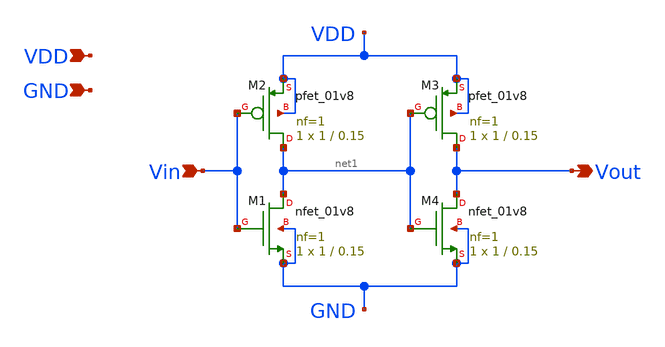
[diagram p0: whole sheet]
** sch_path: xschem/untitled-1.sch
**.subckt untitled-1 Vin VDD GND Vout
*.ipin Vin
*.ipin VDD
*.ipin GND
*.opin Vout
XM1 net1 Vin GND GND sky130_fd_pr__nfet_01v8 L=0.15 W=1 nf=1 ad='int((nf+1)/2) * W/nf * 0.29' as='int((nf+2)/2) * W/nf * 0.29'
+ pd='2*int((nf+1)/2) * (W/nf + 0.29)' ps='2*int((nf+2)/2) * (W/nf + 0.29)' nrd='0.29 / W' nrs='0.29 / W'
+ sa=0 sb=0 sd=0 mult=1 m=1
XM2 net1 Vin VDD VDD sky130_fd_pr__pfet_01v8 L=0.15 W=1 nf=1 ad='int((nf+1)/2) * W/nf * 0.29' as='int((nf+2)/2) * W/nf * 0.29'
+ pd='2*int((nf+1)/2) * (W/nf + 0.29)' ps='2*int((nf+2)/2) * (W/nf + 0.29)' nrd='0.29 / W' nrs='0.29 / W'
+ sa=0 sb=0 sd=0 mult=1 m=1
XM3 Vout net1 VDD VDD sky130_fd_pr__pfet_01v8 L=0.15 W=1 nf=1 ad='int((nf+1)/2) * W/nf * 0.29' as='int((nf+2)/2) * W/nf * 0.29'
+ pd='2*int((nf+1)/2) * (W/nf + 0.29)' ps='2*int((nf+2)/2) * (W/nf + 0.29)' nrd='0.29 / W' nrs='0.29 / W'
+ sa=0 sb=0 sd=0 mult=1 m=1
XM4 Vout net1 GND GND sky130_fd_pr__nfet_01v8 L=0.15 W=1 nf=1 ad='int((nf+1)/2) * W/nf * 0.29' as='int((nf+2)/2) * W/nf * 0.29'
+ pd='2*int((nf+1)/2) * (W/nf + 0.29)' ps='2*int((nf+2)/2) * (W/nf + 0.29)' nrd='0.29 / W' nrs='0.29 / W'
+ sa=0 sb=0 sd=0 mult=1 m=1
**.ends
.end
